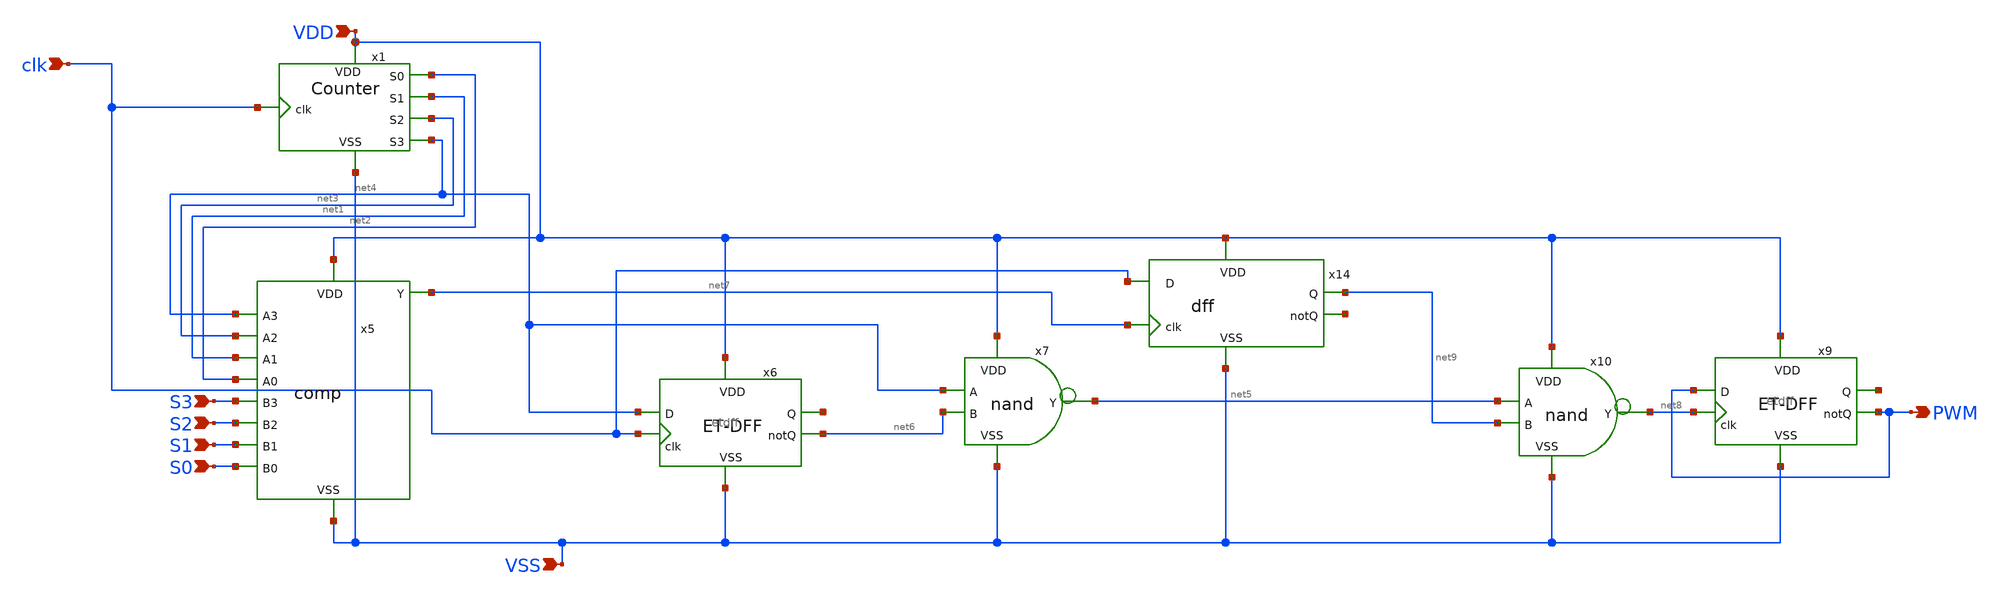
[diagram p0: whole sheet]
** sch_path: Layouts and Schematics/Spice Sim and Schem/xschem_pwm.sch
**.subckt xschem_pwm VDD VSS PWM clk S3 S2 S1 S0
*.ipin VDD
*.ipin VSS
*.opin PWM
*.ipin clk
*.ipin S3
*.ipin S2
*.ipin S1
*.ipin S0
x5 VDD net4 net1 net2 net3 S3 S2 S1 S0 net7 VSS comp
x6 VDD net4 net10 clk net6 VSS etdff
x9 VDD PWM net11 net8 PWM VSS etdff
x10 VDD net5 net8 net9 VSS nand
x14 VDD net7 net9 clk net12 VSS dff
x7 VDD net4 net5 net6 VSS nand
x1 VDD net4 net2 net1 net3 clk VSS count
**.ends
.end
